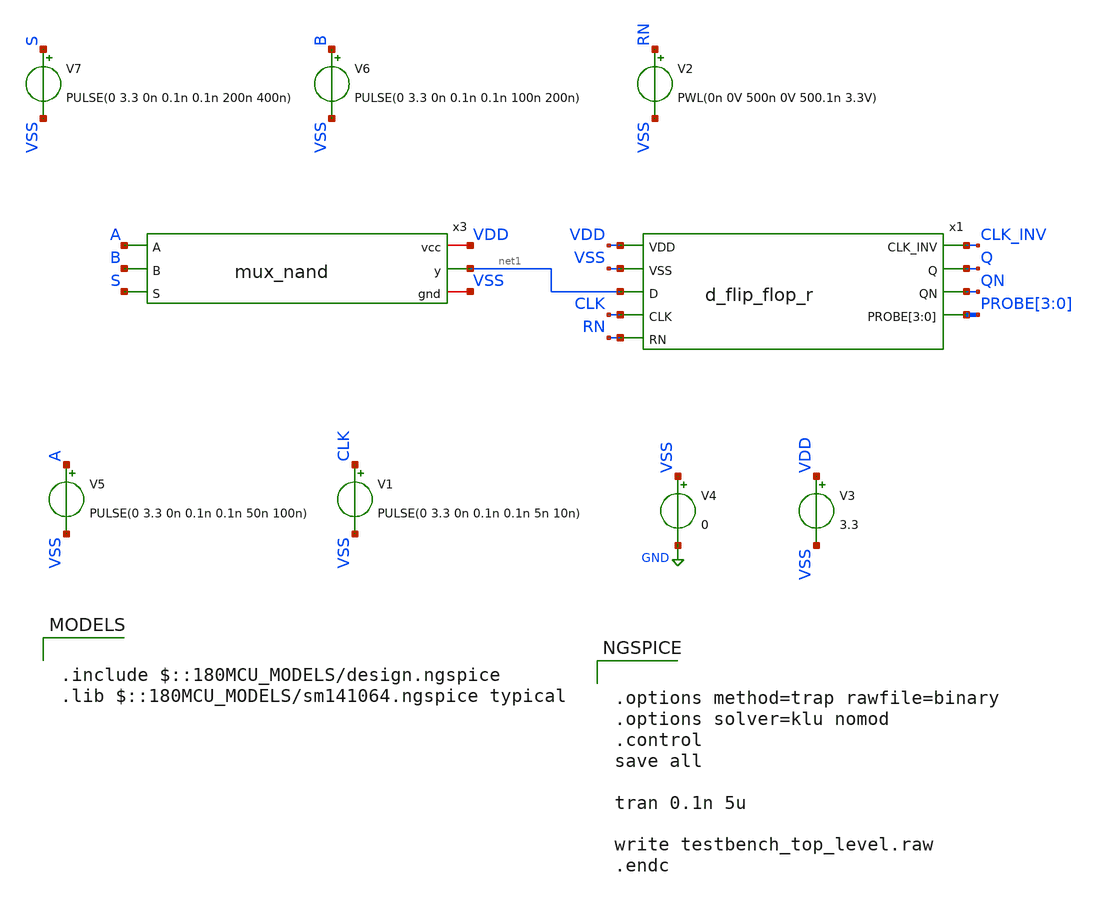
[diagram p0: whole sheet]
** sch_path: designs/schematics/testbench_top_level.sch
**.subckt testbench_top_level
V1 CLK VSS PULSE(0 3.3 0n 0.1n 0.1n 5n 10n)
V3 VDD VSS 3.3
V4 VSS GND 0
V5 A VSS PULSE(0 3.3 0n 0.1n 0.1n 50n 100n)
V6 B VSS PULSE(0 3.3 0n 0.1n 0.1n 100n 200n)
V7 S VSS PULSE(0 3.3 0n 0.1n 0.1n 200n 400n)
V2 RN VSS PWL(0n 0V 500n 0V 500.1n 3.3V)
x3 VDD A net1 B S VSS mux_nand
x1 VDD CLK_INV VSS Q net1 QN CLK PROBE[3] PROBE[2] PROBE[1] PROBE[0] RN d_flip_flop_r
**** begin user architecture code

.include $::180MCU_MODELS/design.ngspice
.lib $::180MCU_MODELS/sm141064.ngspice typical



.options method=trap rawfile=binary
.options solver=klu nomod
.control
save all

tran 0.1n 5u

write testbench_top_level.raw
.endc


**** end user architecture code
**.ends

* expanding   symbol:
*+  /home/raditya/Documents/mySpace/Projects/Chipathon_2025/voidwalkers-scandff-gf180mcu/designs/schematics/mux2x1/mux_nand.sym # of pins=6
** sym_path: designs/libs/mux2x1/mux_nand.sym
** sch_path: designs/libs/mux2x1/mux_nand.sch
.subckt mux_nand vcc A y B S gnd
*.ipin S
*.ipin A
*.ipin B
*.opin y
*.iopin vcc
*.iopin gnd
x1 vcc S net1 gnd inv
x2 vcc net2 A net1 gnd nand
x3 vcc net3 B S gnd nand
x4 vcc y net2 net3 gnd nand
.ends


* expanding   symbol:
*+  /home/raditya/Documents/mySpace/Projects/Chipathon_2025/voidwalkers-scandff-gf180mcu/designs/schematics/d_flip_flop/d_flip_flop_r.sym # of pins=9
** sym_path: designs/schematics/d_flip_flop/d_flip_flop_r.sym
** sch_path: designs/schematics/d_flip_flop/d_flip_flop_r.sch
.subckt d_flip_flop_r VDD CLK_INV VSS Q D QN CLK PROBE[3] PROBE[2] PROBE[1] PROBE[0] RN
*.ipin D
*.ipin VDD
*.ipin VSS
*.opin Q
*.ipin CLK
*.ipin RN
*.opin CLK_INV
*.opin QN
*.opin PROBE[3],PROBE[2],PROBE[1],PROBE[0]
XM1 net1 D VDD VDD pfet_03v3 L=0.3u W=1.7u nf=1 ad='int((nf+1)/2) * W/nf * 0.18u' as='int((nf+2)/2) * W/nf * 0.18u'
+ pd='2*int((nf+1)/2) * (W/nf + 0.18u)' ps='2*int((nf+2)/2) * (W/nf + 0.18u)' nrd='0.18u / W' nrs='0.18u / W'
+ sa=0 sb=0 sd=0 m=1
XM2 PROBE[0] CLK_INV net2 VSS nfet_03v3 L=0.3u W=0.85u nf=1 ad='int((nf+1)/2) * W/nf * 0.18u' as='int((nf+2)/2) * W/nf * 0.18u'
+ pd='2*int((nf+1)/2) * (W/nf + 0.18u)' ps='2*int((nf+2)/2) * (W/nf + 0.18u)' nrd='0.18u / W' nrs='0.18u / W'
+ sa=0 sb=0 sd=0 m=1
XM3 PROBE[0] CLK net1 VDD pfet_03v3 L=0.3u W=1.7u nf=1 ad='int((nf+1)/2) * W/nf * 0.18u' as='int((nf+2)/2) * W/nf * 0.18u'
+ pd='2*int((nf+1)/2) * (W/nf + 0.18u)' ps='2*int((nf+2)/2) * (W/nf + 0.18u)' nrd='0.18u / W' nrs='0.18u / W'
+ sa=0 sb=0 sd=0 m=1
XM4 net2 D VSS VSS nfet_03v3 L=0.3u W=0.85u nf=1 ad='int((nf+1)/2) * W/nf * 0.18u' as='int((nf+2)/2) * W/nf * 0.18u'
+ pd='2*int((nf+1)/2) * (W/nf + 0.18u)' ps='2*int((nf+2)/2) * (W/nf + 0.18u)' nrd='0.18u / W' nrs='0.18u / W'
+ sa=0 sb=0 sd=0 m=1
XM5 CLK_INV CLK VDD VDD pfet_03v3 L=0.3u W=1.7u nf=1 ad='int((nf+1)/2) * W/nf * 0.18u' as='int((nf+2)/2) * W/nf * 0.18u'
+ pd='2*int((nf+1)/2) * (W/nf + 0.18u)' ps='2*int((nf+2)/2) * (W/nf + 0.18u)' nrd='0.18u / W' nrs='0.18u / W'
+ sa=0 sb=0 sd=0 m=1
XM8 CLK_INV CLK VSS VSS nfet_03v3 L=0.3u W=0.85u nf=1 ad='int((nf+1)/2) * W/nf * 0.18u' as='int((nf+2)/2) * W/nf * 0.18u'
+ pd='2*int((nf+1)/2) * (W/nf + 0.18u)' ps='2*int((nf+2)/2) * (W/nf + 0.18u)' nrd='0.18u / W' nrs='0.18u / W'
+ sa=0 sb=0 sd=0 m=1
XM13 net3 PROBE[1] VDD VDD pfet_03v3 L=0.3u W=1.7u nf=1 ad='int((nf+1)/2) * W/nf * 0.18u' as='int((nf+2)/2) * W/nf * 0.18u'
+ pd='2*int((nf+1)/2) * (W/nf + 0.18u)' ps='2*int((nf+2)/2) * (W/nf + 0.18u)' nrd='0.18u / W' nrs='0.18u / W'
+ sa=0 sb=0 sd=0 m=1
XM14 PROBE[0] CLK net4 VSS nfet_03v3 L=0.3u W=0.85u nf=1 ad='int((nf+1)/2) * W/nf * 0.18u' as='int((nf+2)/2) * W/nf * 0.18u'
+ pd='2*int((nf+1)/2) * (W/nf + 0.18u)' ps='2*int((nf+2)/2) * (W/nf + 0.18u)' nrd='0.18u / W' nrs='0.18u / W'
+ sa=0 sb=0 sd=0 m=1
XM15 PROBE[0] CLK_INV net3 VDD pfet_03v3 L=0.3u W=1.7u nf=1 ad='int((nf+1)/2) * W/nf * 0.18u' as='int((nf+2)/2) * W/nf * 0.18u'
+ pd='2*int((nf+1)/2) * (W/nf + 0.18u)' ps='2*int((nf+2)/2) * (W/nf + 0.18u)' nrd='0.18u / W' nrs='0.18u / W'
+ sa=0 sb=0 sd=0 m=1
XM16 net4 PROBE[1] VSS VSS nfet_03v3 L=0.3u W=0.85u nf=1 ad='int((nf+1)/2) * W/nf * 0.18u' as='int((nf+2)/2) * W/nf * 0.18u'
+ pd='2*int((nf+1)/2) * (W/nf + 0.18u)' ps='2*int((nf+2)/2) * (W/nf + 0.18u)' nrd='0.18u / W' nrs='0.18u / W'
+ sa=0 sb=0 sd=0 m=1
XM9 net5 PROBE[1] VDD VDD pfet_03v3 L=0.3u W=1.7u nf=1 ad='int((nf+1)/2) * W/nf * 0.18u' as='int((nf+2)/2) * W/nf * 0.18u'
+ pd='2*int((nf+1)/2) * (W/nf + 0.18u)' ps='2*int((nf+2)/2) * (W/nf + 0.18u)' nrd='0.18u / W' nrs='0.18u / W'
+ sa=0 sb=0 sd=0 m=1
XM10 PROBE[2] CLK net6 VSS nfet_03v3 L=0.3u W=0.85u nf=1 ad='int((nf+1)/2) * W/nf * 0.18u' as='int((nf+2)/2) * W/nf * 0.18u'
+ pd='2*int((nf+1)/2) * (W/nf + 0.18u)' ps='2*int((nf+2)/2) * (W/nf + 0.18u)' nrd='0.18u / W' nrs='0.18u / W'
+ sa=0 sb=0 sd=0 m=1
XM11 PROBE[2] CLK_INV net5 VDD pfet_03v3 L=0.3u W=1.7u nf=1 ad='int((nf+1)/2) * W/nf * 0.18u' as='int((nf+2)/2) * W/nf * 0.18u'
+ pd='2*int((nf+1)/2) * (W/nf + 0.18u)' ps='2*int((nf+2)/2) * (W/nf + 0.18u)' nrd='0.18u / W' nrs='0.18u / W'
+ sa=0 sb=0 sd=0 m=1
XM12 net6 PROBE[1] VSS VSS nfet_03v3 L=0.3u W=0.85u nf=1 ad='int((nf+1)/2) * W/nf * 0.18u' as='int((nf+2)/2) * W/nf * 0.18u'
+ pd='2*int((nf+1)/2) * (W/nf + 0.18u)' ps='2*int((nf+2)/2) * (W/nf + 0.18u)' nrd='0.18u / W' nrs='0.18u / W'
+ sa=0 sb=0 sd=0 m=1
XM19 net7 PROBE[3] VDD VDD pfet_03v3 L=0.3u W=1.7u nf=1 ad='int((nf+1)/2) * W/nf * 0.18u' as='int((nf+2)/2) * W/nf * 0.18u'
+ pd='2*int((nf+1)/2) * (W/nf + 0.18u)' ps='2*int((nf+2)/2) * (W/nf + 0.18u)' nrd='0.18u / W' nrs='0.18u / W'
+ sa=0 sb=0 sd=0 m=1
XM20 PROBE[2] CLK_INV net8 VSS nfet_03v3 L=0.3u W=0.85u nf=1 ad='int((nf+1)/2) * W/nf * 0.18u' as='int((nf+2)/2) * W/nf * 0.18u'
+ pd='2*int((nf+1)/2) * (W/nf + 0.18u)' ps='2*int((nf+2)/2) * (W/nf + 0.18u)' nrd='0.18u / W' nrs='0.18u / W'
+ sa=0 sb=0 sd=0 m=1
XM21 PROBE[2] CLK net7 VDD pfet_03v3 L=0.3u W=1.7u nf=1 ad='int((nf+1)/2) * W/nf * 0.18u' as='int((nf+2)/2) * W/nf * 0.18u'
+ pd='2*int((nf+1)/2) * (W/nf + 0.18u)' ps='2*int((nf+2)/2) * (W/nf + 0.18u)' nrd='0.18u / W' nrs='0.18u / W'
+ sa=0 sb=0 sd=0 m=1
XM22 net8 PROBE[3] VSS VSS nfet_03v3 L=0.3u W=0.85u nf=1 ad='int((nf+1)/2) * W/nf * 0.18u' as='int((nf+2)/2) * W/nf * 0.18u'
+ pd='2*int((nf+1)/2) * (W/nf + 0.18u)' ps='2*int((nf+2)/2) * (W/nf + 0.18u)' nrd='0.18u / W' nrs='0.18u / W'
+ sa=0 sb=0 sd=0 m=1
XM23 QN PROBE[3] VDD VDD pfet_03v3 L=0.3u W=1.7u nf=1 ad='int((nf+1)/2) * W/nf * 0.18u' as='int((nf+2)/2) * W/nf * 0.18u'
+ pd='2*int((nf+1)/2) * (W/nf + 0.18u)' ps='2*int((nf+2)/2) * (W/nf + 0.18u)' nrd='0.18u / W' nrs='0.18u / W'
+ sa=0 sb=0 sd=0 m=1
XM24 QN PROBE[3] VSS VSS nfet_03v3 L=0.3u W=0.85u nf=1 ad='int((nf+1)/2) * W/nf * 0.18u' as='int((nf+2)/2) * W/nf * 0.18u'
+ pd='2*int((nf+1)/2) * (W/nf + 0.18u)' ps='2*int((nf+2)/2) * (W/nf + 0.18u)' nrd='0.18u / W' nrs='0.18u / W'
+ sa=0 sb=0 sd=0 m=1
XM25 Q QN VDD VDD pfet_03v3 L=0.3u W=1.7u nf=1 ad='int((nf+1)/2) * W/nf * 0.18u' as='int((nf+2)/2) * W/nf * 0.18u'
+ pd='2*int((nf+1)/2) * (W/nf + 0.18u)' ps='2*int((nf+2)/2) * (W/nf + 0.18u)' nrd='0.18u / W' nrs='0.18u / W'
+ sa=0 sb=0 sd=0 m=1
XM26 Q QN VSS VSS nfet_03v3 L=0.3u W=0.85u nf=1 ad='int((nf+1)/2) * W/nf * 0.18u' as='int((nf+2)/2) * W/nf * 0.18u'
+ pd='2*int((nf+1)/2) * (W/nf + 0.18u)' ps='2*int((nf+2)/2) * (W/nf + 0.18u)' nrd='0.18u / W' nrs='0.18u / W'
+ sa=0 sb=0 sd=0 m=1
XM6 net9 PROBE[0] VDD VDD pfet_03v3 L=0.3u W=1.7u nf=1 ad='int((nf+1)/2) * W/nf * 0.18u' as='int((nf+2)/2) * W/nf * 0.18u'
+ pd='2*int((nf+1)/2) * (W/nf + 0.18u)' ps='2*int((nf+2)/2) * (W/nf + 0.18u)' nrd='0.18u / W' nrs='0.18u / W'
+ sa=0 sb=0 sd=0 m=1
XM27 PROBE[1] RN net9 VDD pfet_03v3 L=0.3u W=1.7u nf=1 ad='int((nf+1)/2) * W/nf * 0.18u' as='int((nf+2)/2) * W/nf * 0.18u'
+ pd='2*int((nf+1)/2) * (W/nf + 0.18u)' ps='2*int((nf+2)/2) * (W/nf + 0.18u)' nrd='0.18u / W' nrs='0.18u / W'
+ sa=0 sb=0 sd=0 m=1
XM28 PROBE[1] PROBE[0] VSS VSS nfet_03v3 L=0.3u W=0.85u nf=1 ad='int((nf+1)/2) * W/nf * 0.18u' as='int((nf+2)/2) * W/nf * 0.18u'
+ pd='2*int((nf+1)/2) * (W/nf + 0.18u)' ps='2*int((nf+2)/2) * (W/nf + 0.18u)' nrd='0.18u / W' nrs='0.18u / W'
+ sa=0 sb=0 sd=0 m=1
XM17 net10 PROBE[2] VDD VDD pfet_03v3 L=0.3u W=1.7u nf=1 ad='int((nf+1)/2) * W/nf * 0.18u' as='int((nf+2)/2) * W/nf * 0.18u'
+ pd='2*int((nf+1)/2) * (W/nf + 0.18u)' ps='2*int((nf+2)/2) * (W/nf + 0.18u)' nrd='0.18u / W' nrs='0.18u / W'
+ sa=0 sb=0 sd=0 m=1
XM29 PROBE[3] RN net10 VDD pfet_03v3 L=0.3u W=1.7u nf=1 ad='int((nf+1)/2) * W/nf * 0.18u' as='int((nf+2)/2) * W/nf * 0.18u'
+ pd='2*int((nf+1)/2) * (W/nf + 0.18u)' ps='2*int((nf+2)/2) * (W/nf + 0.18u)' nrd='0.18u / W' nrs='0.18u / W'
+ sa=0 sb=0 sd=0 m=1
XM30 PROBE[3] PROBE[2] VSS VSS nfet_03v3 L=0.3u W=0.85u nf=1 ad='int((nf+1)/2) * W/nf * 0.18u' as='int((nf+2)/2) * W/nf * 0.18u'
+ pd='2*int((nf+1)/2) * (W/nf + 0.18u)' ps='2*int((nf+2)/2) * (W/nf + 0.18u)' nrd='0.18u / W' nrs='0.18u / W'
+ sa=0 sb=0 sd=0 m=1
XM7 PROBE[1] RN VSS VSS nfet_03v3 L=0.3u W=0.85u nf=1 ad='int((nf+1)/2) * W/nf * 0.18u' as='int((nf+2)/2) * W/nf * 0.18u'
+ pd='2*int((nf+1)/2) * (W/nf + 0.18u)' ps='2*int((nf+2)/2) * (W/nf + 0.18u)' nrd='0.18u / W' nrs='0.18u / W'
+ sa=0 sb=0 sd=0 m=1
XM18 PROBE[3] RN VSS VSS nfet_03v3 L=0.3u W=0.85u nf=1 ad='int((nf+1)/2) * W/nf * 0.18u' as='int((nf+2)/2) * W/nf * 0.18u'
+ pd='2*int((nf+1)/2) * (W/nf + 0.18u)' ps='2*int((nf+2)/2) * (W/nf + 0.18u)' nrd='0.18u / W' nrs='0.18u / W'
+ sa=0 sb=0 sd=0 m=1
.ends


* expanding   symbol:  voidwalkers-scandff-gf180mcu/designs/libs/mux2x1/inv.sym # of pins=4
** sym_path: designs/schematics/mux2x1/inv.sym
** sch_path: designs/schematics/mux2x1/inv.sch
.subckt inv vcc in out gnd
*.ipin in
*.opin out
*.iopin vcc
*.iopin gnd
XM2 out in vcc vcc pfet_03v3 L=0.28u W=0.22u nf=1 ad='int((nf+1)/2) * W/nf * 0.18u' as='int((nf+2)/2) * W/nf * 0.18u'
+ pd='2*int((nf+1)/2) * (W/nf + 0.18u)' ps='2*int((nf+2)/2) * (W/nf + 0.18u)' nrd='0.18u / W' nrs='0.18u / W'
+ sa=0 sb=0 sd=0 m=1
XM1 out in gnd gnd nfet_03v3 L=0.28u W=0.22u nf=1 ad='int((nf+1)/2) * W/nf * 0.18u' as='int((nf+2)/2) * W/nf * 0.18u'
+ pd='2*int((nf+1)/2) * (W/nf + 0.18u)' ps='2*int((nf+2)/2) * (W/nf + 0.18u)' nrd='0.18u / W' nrs='0.18u / W'
+ sa=0 sb=0 sd=0 m=1
.ends


* expanding   symbol:  voidwalkers-scandff-gf180mcu/designs/libs/mux2x1/nand.sym # of pins=5
** sym_path: designs/schematics/mux2x1/nand.sym
** sch_path: designs/schematics/mux2x1/nand.sch
.subckt nand vcc OUT A B gnd
*.ipin A
*.ipin B
*.opin OUT
*.iopin vcc
*.iopin gnd
XM1 OUT B net1 gnd nfet_03v3 L=0.28u W=0.22u nf=1 ad='int((nf+1)/2) * W/nf * 0.18u' as='int((nf+2)/2) * W/nf * 0.18u'
+ pd='2*int((nf+1)/2) * (W/nf + 0.18u)' ps='2*int((nf+2)/2) * (W/nf + 0.18u)' nrd='0.18u / W' nrs='0.18u / W'
+ sa=0 sb=0 sd=0 m=1
XM2 net1 A gnd gnd nfet_03v3 L=0.28u W=0.22u nf=1 ad='int((nf+1)/2) * W/nf * 0.18u' as='int((nf+2)/2) * W/nf * 0.18u'
+ pd='2*int((nf+1)/2) * (W/nf + 0.18u)' ps='2*int((nf+2)/2) * (W/nf + 0.18u)' nrd='0.18u / W' nrs='0.18u / W'
+ sa=0 sb=0 sd=0 m=1
XM3 OUT A vcc vcc pfet_03v3 L=0.28u W=0.22u nf=1 ad='int((nf+1)/2) * W/nf * 0.18u' as='int((nf+2)/2) * W/nf * 0.18u'
+ pd='2*int((nf+1)/2) * (W/nf + 0.18u)' ps='2*int((nf+2)/2) * (W/nf + 0.18u)' nrd='0.18u / W' nrs='0.18u / W'
+ sa=0 sb=0 sd=0 m=1
XM4 OUT B vcc vcc pfet_03v3 L=0.28u W=0.22u nf=1 ad='int((nf+1)/2) * W/nf * 0.18u' as='int((nf+2)/2) * W/nf * 0.18u'
+ pd='2*int((nf+1)/2) * (W/nf + 0.18u)' ps='2*int((nf+2)/2) * (W/nf + 0.18u)' nrd='0.18u / W' nrs='0.18u / W'
+ sa=0 sb=0 sd=0 m=1
.ends

.GLOBAL GND
.end
